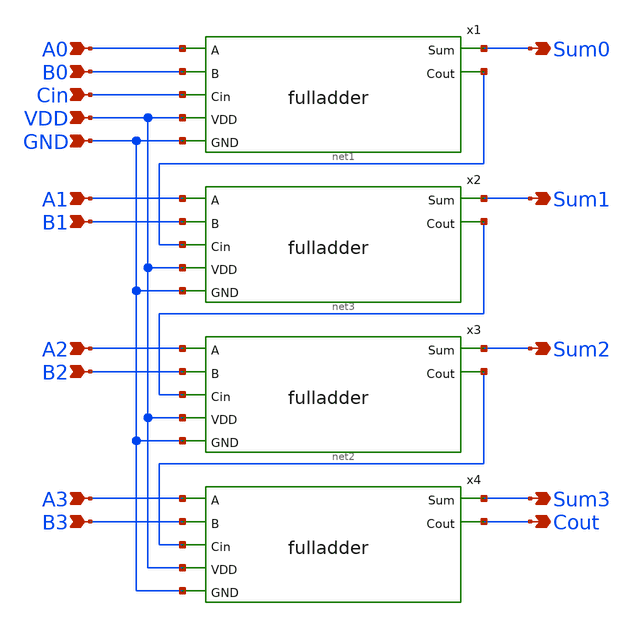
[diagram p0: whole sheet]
** sch_path: transmission_gate/schematic/fulladder_4bit.sch
**.subckt fulladder_4bit A0 B0 Cin VDD GND A1 B1 A2 B2 A3 B3 Sum0 Sum1 Sum2 Sum3 Cout
*.ipin A0
*.ipin B0
*.ipin Cin
*.ipin VDD
*.ipin GND
*.ipin A1
*.ipin B1
*.ipin A2
*.ipin B2
*.ipin A3
*.ipin B3
*.opin Sum0
*.opin Sum1
*.opin Sum2
*.opin Sum3
*.opin Cout
x1 A0 Sum0 B0 Cin VDD net1 GND fulladder
x2 A1 Sum1 B1 net1 VDD net3 GND fulladder
x3 A2 Sum2 B2 net3 VDD net2 GND fulladder
x4 A3 Sum3 B3 net2 VDD Cout GND fulladder
**.ends

* expanding   symbol:
*+  /home/dat02/projects/cmos-full-adder-sky130/transmission_gate/schematic/fulladder.sym # of pins=7
** sym_path: transmission_gate/schematic/fulladder.sym
** sch_path: transmission_gate/schematic/fulladder.sch
.subckt fulladder A Sum B Cin VDD Cout GND
*.opin Cout
*.ipin A
*.ipin B
*.ipin Cin
*.opin Sum
*.ipin VDD
*.ipin GND
XM1 Cout net4 A VDD sky130_fd_pr__pfet_01v8 L=0.15 W=1.295 nf=1 ad='int((1 + 1)/2) * 1.295 / 1 * 0.29'
+ as='int((1 + 2)/2) * 1.295 / 1 * 0.29' pd='2*int((1 + 1)/2) * (1.295 / 1 + 0.29)' ps='2*int((1 + 2)/2) * (1.295 / 1 + 0.29)'
+ nrd='0.29 / 1.295 ' nrs='0.29 / 1.295 ' sa=0 sb=0 sd=0 mult=1 m=1
XM2 Cout net1 A GND sky130_fd_pr__nfet_01v8 L=0.15 W=0.42 nf=1 ad='int((1 + 1)/2) * 0.42 / 1 * 0.29'
+ as='int((1 + 2)/2) * 0.42 / 1 * 0.29' pd='2*int((1 + 1)/2) * (0.42 / 1 + 0.29)' ps='2*int((1 + 2)/2) * (0.42 / 1 + 0.29)'
+ nrd='0.29 / 0.42 ' nrs='0.29 / 0.42 ' sa=0 sb=0 sd=0 mult=1 m=1
XM3 Cout net1 Cin VDD sky130_fd_pr__pfet_01v8 L=0.15 W=1.295 nf=1 ad='int((1 + 1)/2) * 1.295 / 1 * 0.29'
+ as='int((1 + 2)/2) * 1.295 / 1 * 0.29' pd='2*int((1 + 1)/2) * (1.295 / 1 + 0.29)' ps='2*int((1 + 2)/2) * (1.295 / 1 + 0.29)'
+ nrd='0.29 / 1.295 ' nrs='0.29 / 1.295 ' sa=0 sb=0 sd=0 mult=1 m=1
XM4 Cout net4 Cin GND sky130_fd_pr__nfet_01v8 L=0.15 W=0.42 nf=1 ad='int((1 + 1)/2) * 0.42 / 1 * 0.29'
+ as='int((1 + 2)/2) * 0.42 / 1 * 0.29' pd='2*int((1 + 1)/2) * (0.42 / 1 + 0.29)' ps='2*int((1 + 2)/2) * (0.42 / 1 + 0.29)'
+ nrd='0.29 / 0.42 ' nrs='0.29 / 0.42 ' sa=0 sb=0 sd=0 mult=1 m=1
XM7 net2 A VDD VDD sky130_fd_pr__pfet_01v8 L=0.15 W=1.885 nf=1 ad='int((1 + 1)/2) * 1.885 / 1 * 0.29'
+ as='int((1 + 2)/2) * 1.885 / 1 * 0.29' pd='2*int((1 + 1)/2) * (1.885 / 1 + 0.29)' ps='2*int((1 + 2)/2) * (1.885 / 1 + 0.29)'
+ nrd='0.29 / 1.885 ' nrs='0.29 / 1.885 ' sa=0 sb=0 sd=0 mult=1 m=1
XM8 net2 A GND GND sky130_fd_pr__nfet_01v8 L=0.15 W=0.61 nf=1 ad='int((1 + 1)/2) * 0.61 / 1 * 0.29' as='int((1 + 2)/2) * 0.61 / 1 * 0.29'
+ pd='2*int((1 + 1)/2) * (0.61 / 1 + 0.29)' ps='2*int((1 + 2)/2) * (0.61 / 1 + 0.29)' nrd='0.29 / 0.61 '
+ nrs='0.29 / 0.61 ' sa=0 sb=0 sd=0 mult=1 m=1
XM9 net3 B VDD VDD sky130_fd_pr__pfet_01v8 L=0.15 W=1.885 nf=1 ad='int((1 + 1)/2) * 1.885 / 1 * 0.29'
+ as='int((1 + 2)/2) * 1.885 / 1 * 0.29' pd='2*int((1 + 1)/2) * (1.885 / 1 + 0.29)' ps='2*int((1 + 2)/2) * (1.885 / 1 + 0.29)'
+ nrd='0.29 / 1.885 ' nrs='0.29 / 1.885 ' sa=0 sb=0 sd=0 mult=1 m=1
XM10 net3 B GND GND sky130_fd_pr__nfet_01v8 L=0.15 W=0.61 nf=1 ad='int((1 + 1)/2) * 0.61 / 1 * 0.29'
+ as='int((1 + 2)/2) * 0.61 / 1 * 0.29' pd='2*int((1 + 1)/2) * (0.61 / 1 + 0.29)' ps='2*int((1 + 2)/2) * (0.61 / 1 + 0.29)'
+ nrd='0.29 / 0.61 ' nrs='0.29 / 0.61 ' sa=0 sb=0 sd=0 mult=1 m=1
XM11 net4 A B VDD sky130_fd_pr__pfet_01v8 L=0.15 W=1.885 nf=1 ad='int((1 + 1)/2) * 1.885 / 1 * 0.29'
+ as='int((1 + 2)/2) * 1.885 / 1 * 0.29' pd='2*int((1 + 1)/2) * (1.885 / 1 + 0.29)' ps='2*int((1 + 2)/2) * (1.885 / 1 + 0.29)'
+ nrd='0.29 / 1.885 ' nrs='0.29 / 1.885 ' sa=0 sb=0 sd=0 mult=1 m=1
XM12 net4 net2 B GND sky130_fd_pr__nfet_01v8 L=0.15 W=0.61 nf=1 ad='int((1 + 1)/2) * 0.61 / 1 * 0.29'
+ as='int((1 + 2)/2) * 0.61 / 1 * 0.29' pd='2*int((1 + 1)/2) * (0.61 / 1 + 0.29)' ps='2*int((1 + 2)/2) * (0.61 / 1 + 0.29)'
+ nrd='0.29 / 0.61 ' nrs='0.29 / 0.61 ' sa=0 sb=0 sd=0 mult=1 m=1
XM13 net4 net2 net3 VDD sky130_fd_pr__pfet_01v8 L=0.15 W=1.885 nf=1 ad='int((1 + 1)/2) * 1.885 / 1 * 0.29'
+ as='int((1 + 2)/2) * 1.885 / 1 * 0.29' pd='2*int((1 + 1)/2) * (1.885 / 1 + 0.29)' ps='2*int((1 + 2)/2) * (1.885 / 1 + 0.29)'
+ nrd='0.29 / 1.885 ' nrs='0.29 / 1.885 ' sa=0 sb=0 sd=0 mult=1 m=1
XM14 net4 A net3 GND sky130_fd_pr__nfet_01v8 L=0.15 W=0.61 nf=1 ad='int((1 + 1)/2) * 0.61 / 1 * 0.29'
+ as='int((1 + 2)/2) * 0.61 / 1 * 0.29' pd='2*int((1 + 1)/2) * (0.61 / 1 + 0.29)' ps='2*int((1 + 2)/2) * (0.61 / 1 + 0.29)'
+ nrd='0.29 / 0.61 ' nrs='0.29 / 0.61 ' sa=0 sb=0 sd=0 mult=1 m=1
XM15 net1 net4 VDD VDD sky130_fd_pr__pfet_01v8 L=0.15 W=2.59 nf=1 ad='int((1 + 1)/2) * 2.59 / 1 * 0.29'
+ as='int((1 + 2)/2) * 2.59 / 1 * 0.29' pd='2*int((1 + 1)/2) * (2.59 / 1 + 0.29)' ps='2*int((1 + 2)/2) * (2.59 / 1 + 0.29)'
+ nrd='0.29 / 2.59 ' nrs='0.29 / 2.59 ' sa=0 sb=0 sd=0 mult=1 m=1
XM16 net1 net4 GND GND sky130_fd_pr__nfet_01v8 L=0.15 W=0.84 nf=1 ad='int((1 + 1)/2) * 0.84 / 1 * 0.29'
+ as='int((1 + 2)/2) * 0.84 / 1 * 0.29' pd='2*int((1 + 1)/2) * (0.84 / 1 + 0.29)' ps='2*int((1 + 2)/2) * (0.84 / 1 + 0.29)'
+ nrd='0.29 / 0.84 ' nrs='0.29 / 0.84 ' sa=0 sb=0 sd=0 mult=1 m=1
XM17 net5 Cin VDD VDD sky130_fd_pr__pfet_01v8 L=0.15 W=1.295 nf=1 ad='int((1 + 1)/2) * 1.295 / 1 * 0.29'
+ as='int((1 + 2)/2) * 1.295 / 1 * 0.29' pd='2*int((1 + 1)/2) * (1.295 / 1 + 0.29)' ps='2*int((1 + 2)/2) * (1.295 / 1 + 0.29)'
+ nrd='0.29 / 1.295 ' nrs='0.29 / 1.295 ' sa=0 sb=0 sd=0 mult=1 m=1
XM18 net5 Cin GND GND sky130_fd_pr__nfet_01v8 L=0.15 W=0.42 nf=1 ad='int((1 + 1)/2) * 0.42 / 1 * 0.29'
+ as='int((1 + 2)/2) * 0.42 / 1 * 0.29' pd='2*int((1 + 1)/2) * (0.42 / 1 + 0.29)' ps='2*int((1 + 2)/2) * (0.42 / 1 + 0.29)'
+ nrd='0.29 / 0.42 ' nrs='0.29 / 0.42 ' sa=0 sb=0 sd=0 mult=1 m=1
XM19 Sum net4 Cin VDD sky130_fd_pr__pfet_01v8 L=0.15 W=1.295 nf=1 ad='int((1 + 1)/2) * 1.295 / 1 * 0.29'
+ as='int((1 + 2)/2) * 1.295 / 1 * 0.29' pd='2*int((1 + 1)/2) * (1.295 / 1 + 0.29)' ps='2*int((1 + 2)/2) * (1.295 / 1 + 0.29)'
+ nrd='0.29 / 1.295 ' nrs='0.29 / 1.295 ' sa=0 sb=0 sd=0 mult=1 m=1
XM20 Sum net1 Cin GND sky130_fd_pr__nfet_01v8 L=0.15 W=0.42 nf=1 ad='int((1 + 1)/2) * 0.42 / 1 * 0.29'
+ as='int((1 + 2)/2) * 0.42 / 1 * 0.29' pd='2*int((1 + 1)/2) * (0.42 / 1 + 0.29)' ps='2*int((1 + 2)/2) * (0.42 / 1 + 0.29)'
+ nrd='0.29 / 0.42 ' nrs='0.29 / 0.42 ' sa=0 sb=0 sd=0 mult=1 m=1
XM21 Sum net1 net5 VDD sky130_fd_pr__pfet_01v8 L=0.15 W=1.295 nf=1 ad='int((1 + 1)/2) * 1.295 / 1 * 0.29'
+ as='int((1 + 2)/2) * 1.295 / 1 * 0.29' pd='2*int((1 + 1)/2) * (1.295 / 1 + 0.29)' ps='2*int((1 + 2)/2) * (1.295 / 1 + 0.29)'
+ nrd='0.29 / 1.295 ' nrs='0.29 / 1.295 ' sa=0 sb=0 sd=0 mult=1 m=1
XM22 Sum net4 net5 GND sky130_fd_pr__nfet_01v8 L=0.15 W=0.42 nf=1 ad='int((1 + 1)/2) * 0.42 / 1 * 0.29'
+ as='int((1 + 2)/2) * 0.42 / 1 * 0.29' pd='2*int((1 + 1)/2) * (0.42 / 1 + 0.29)' ps='2*int((1 + 2)/2) * (0.42 / 1 + 0.29)'
+ nrd='0.29 / 0.42 ' nrs='0.29 / 0.42 ' sa=0 sb=0 sd=0 mult=1 m=1
.ends

.GLOBAL GND
.GLOBAL VDD
.end
